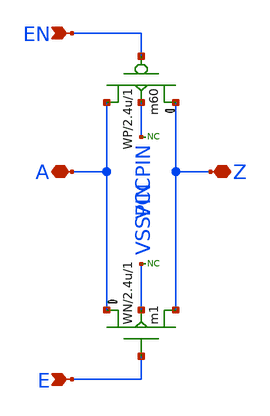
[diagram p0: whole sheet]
** sch_path: xschem_libs_newsym/rom8k/passhs/schematic/passhs.sch
* Copyright (C) 1998-2024 Stefan Frederik Schippers
* This program is free software; you can redistribute it and/or modify
* it under the terms of the GNU General Public License as published by
* the Free Software Foundation; either version 2 of the License, or
* (at your option) any later version.
* This program is distributed in the hope that it will be useful,
* but WITHOUT ANY WARRANTY; without even the implied warranty of
* MERCHANTABILITY or FITNESS FOR A PARTICULAR PURPOSE.  See the
* GNU General Public License for more details.
* You should have received a copy of the GNU General Public License
* along with this program; if not, write to the Free Software
**.subckt passhs Z A EN E
*.iopin Z
*.iopin A
*.ipin EN
*.ipin E
m60 Z EN A VCCPIN cmosp w=WP l=2.4u ad='WP *4.6u' as='WP *4.6u' pd='WP *2+9.2u' ps='WP *2+9.2u' m=1
m1 A E Z VSSPIN cmosn w=WN l=2.4u ad='WN *4.3u' as='WN *4.3u' pd='WN *2+8.6u' ps='WN *2+8.6u' m=1
* noconn VSSPIN
* noconn VCCPIN
**.ends
.end
